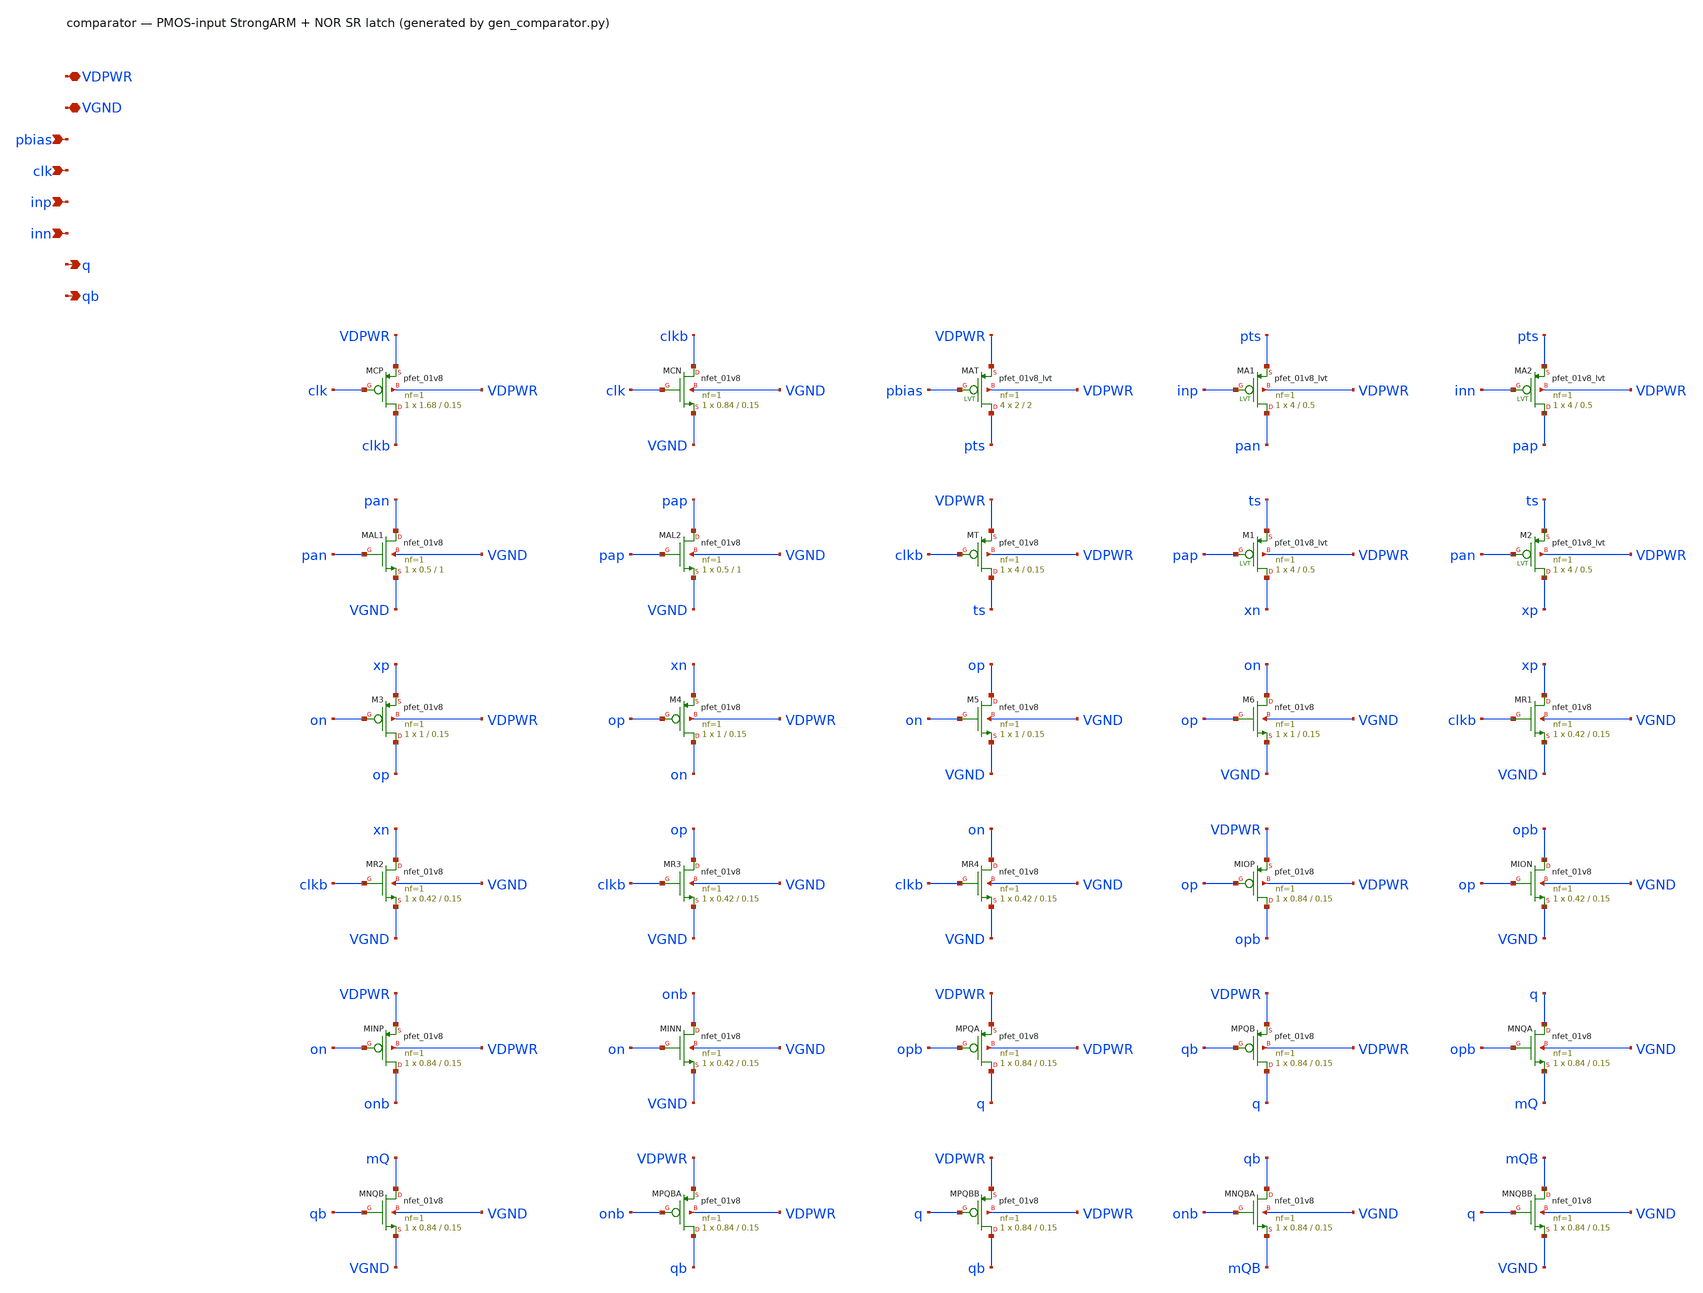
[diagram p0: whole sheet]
** sch_path: xschem/comparator.sch
**.subckt comparator VDPWR VGND pbias clk inp inn q qb
*.iopin VDPWR
*.iopin VGND
*.ipin pbias
*.ipin clk
*.ipin inp
*.ipin inn
*.opin q
*.opin qb
XMCP clkb clk VDPWR VDPWR sky130_fd_pr__pfet_01v8 L=0.15 W=1.68 nf=1 ad='int((nf+1)/2) * W/nf * 0.29'
+ as='int((nf+2)/2) * W/nf * 0.29' pd='2*int((nf+1)/2) * (W/nf + 0.29)' ps='2*int((nf+2)/2) * (W/nf + 0.29)'
+ nrd='0.29 / W' nrs='0.29 / W' sa=0 sb=0 sd=0 mult=1 m=1
XMCN clkb clk VGND VGND sky130_fd_pr__nfet_01v8 L=0.15 W=0.84 nf=1 ad='int((1 + 1)/2) * 0.84 / 1 * 0.29'
+ as='int((1 + 2)/2) * 0.84 / 1 * 0.29' pd='2*int((1 + 1)/2) * (0.84 / 1 + 0.29)' ps='2*int((1 + 2)/2) * (0.84 / 1 + 0.29)'
+ nrd='0.29 / 0.84 ' nrs='0.29 / 0.84 ' sa=0 sb=0 sd=0 mult=1 m=1
XMAT pts pbias VDPWR VDPWR sky130_fd_pr__pfet_01v8_lvt L=2 W=2 nf=1 ad='int((1 + 1)/2) * 2 / 1 * 0.29'
+ as='int((1 + 2)/2) * 2 / 1 * 0.29' pd='2*int((1 + 1)/2) * (2 / 1 + 0.29)' ps='2*int((1 + 2)/2) * (2 / 1 + 0.29)'
+ nrd='0.29 / 2 ' nrs='0.29 / 2 ' sa=0 sb=0 sd=0 mult=4 m=4
XMA1 pan inp pts VDPWR sky130_fd_pr__pfet_01v8_lvt L=0.5 W=4 nf=1 ad='int((1 + 1)/2) * 4 / 1 * 0.29'
+ as='int((1 + 2)/2) * 4 / 1 * 0.29' pd='2*int((1 + 1)/2) * (4 / 1 + 0.29)' ps='2*int((1 + 2)/2) * (4 / 1 + 0.29)'
+ nrd='0.29 / 4 ' nrs='0.29 / 4 ' sa=0 sb=0 sd=0 mult=1 m=1
XMA2 pap inn pts VDPWR sky130_fd_pr__pfet_01v8_lvt L=0.5 W=4 nf=1 ad='int((1 + 1)/2) * 4 / 1 * 0.29'
+ as='int((1 + 2)/2) * 4 / 1 * 0.29' pd='2*int((1 + 1)/2) * (4 / 1 + 0.29)' ps='2*int((1 + 2)/2) * (4 / 1 + 0.29)'
+ nrd='0.29 / 4 ' nrs='0.29 / 4 ' sa=0 sb=0 sd=0 mult=1 m=1
XMAL1 pan pan VGND VGND sky130_fd_pr__nfet_01v8 L=1 W=0.5 nf=1 ad='int((1 + 1)/2) * 0.5 / 1 * 0.29' as='int((1 + 2)/2) * 0.5 / 1 * 0.29'
+ pd='2*int((1 + 1)/2) * (0.5 / 1 + 0.29)' ps='2*int((1 + 2)/2) * (0.5 / 1 + 0.29)' nrd='0.29 / 0.5 ' nrs='0.29 / 0.5 '
+ sa=0 sb=0 sd=0 mult=1 m=1
XMAL2 pap pap VGND VGND sky130_fd_pr__nfet_01v8 L=1 W=0.5 nf=1 ad='int((1 + 1)/2) * 0.5 / 1 * 0.29' as='int((1 + 2)/2) * 0.5 / 1 * 0.29'
+ pd='2*int((1 + 1)/2) * (0.5 / 1 + 0.29)' ps='2*int((1 + 2)/2) * (0.5 / 1 + 0.29)' nrd='0.29 / 0.5 ' nrs='0.29 / 0.5 '
+ sa=0 sb=0 sd=0 mult=1 m=1
XMT ts clkb VDPWR VDPWR sky130_fd_pr__pfet_01v8 L=0.15 W=4 nf=1 ad='int((nf+1)/2) * W/nf * 0.29' as='int((nf+2)/2) * W/nf * 0.29'
+ pd='2*int((nf+1)/2) * (W/nf + 0.29)' ps='2*int((nf+2)/2) * (W/nf + 0.29)' nrd='0.29 / W' nrs='0.29 / W'
+ sa=0 sb=0 sd=0 mult=1 m=1
XM1 xn pap ts VDPWR sky130_fd_pr__pfet_01v8_lvt L=0.5 W=4 nf=1 ad='int((1 + 1)/2) * 4 / 1 * 0.29' as='int((1 + 2)/2) * 4 / 1 * 0.29'
+ pd='2*int((1 + 1)/2) * (4 / 1 + 0.29)' ps='2*int((1 + 2)/2) * (4 / 1 + 0.29)' nrd='0.29 / 4 ' nrs='0.29 / 4 '
+ sa=0 sb=0 sd=0 mult=1 m=1
XM2 xp pan ts VDPWR sky130_fd_pr__pfet_01v8_lvt L=0.5 W=4 nf=1 ad='int((1 + 1)/2) * 4 / 1 * 0.29' as='int((1 + 2)/2) * 4 / 1 * 0.29'
+ pd='2*int((1 + 1)/2) * (4 / 1 + 0.29)' ps='2*int((1 + 2)/2) * (4 / 1 + 0.29)' nrd='0.29 / 4 ' nrs='0.29 / 4 '
+ sa=0 sb=0 sd=0 mult=1 m=1
XM3 op on xp VDPWR sky130_fd_pr__pfet_01v8 L=0.15 W=1 nf=1 ad='int((nf+1)/2) * W/nf * 0.29' as='int((nf+2)/2) * W/nf * 0.29'
+ pd='2*int((nf+1)/2) * (W/nf + 0.29)' ps='2*int((nf+2)/2) * (W/nf + 0.29)' nrd='0.29 / W' nrs='0.29 / W'
+ sa=0 sb=0 sd=0 mult=1 m=1
XM4 on op xn VDPWR sky130_fd_pr__pfet_01v8 L=0.15 W=1 nf=1 ad='int((nf+1)/2) * W/nf * 0.29' as='int((nf+2)/2) * W/nf * 0.29'
+ pd='2*int((nf+1)/2) * (W/nf + 0.29)' ps='2*int((nf+2)/2) * (W/nf + 0.29)' nrd='0.29 / W' nrs='0.29 / W'
+ sa=0 sb=0 sd=0 mult=1 m=1
XM5 op on VGND VGND sky130_fd_pr__nfet_01v8 L=0.15 W=1 nf=1 ad='int((1 + 1)/2) * 1 / 1 * 0.29' as='int((1 + 2)/2) * 1 / 1 * 0.29'
+ pd='2*int((1 + 1)/2) * (1 / 1 + 0.29)' ps='2*int((1 + 2)/2) * (1 / 1 + 0.29)' nrd='0.29 / 1 ' nrs='0.29 / 1 '
+ sa=0 sb=0 sd=0 mult=1 m=1
XM6 on op VGND VGND sky130_fd_pr__nfet_01v8 L=0.15 W=1 nf=1 ad='int((1 + 1)/2) * 1 / 1 * 0.29' as='int((1 + 2)/2) * 1 / 1 * 0.29'
+ pd='2*int((1 + 1)/2) * (1 / 1 + 0.29)' ps='2*int((1 + 2)/2) * (1 / 1 + 0.29)' nrd='0.29 / 1 ' nrs='0.29 / 1 '
+ sa=0 sb=0 sd=0 mult=1 m=1
XMR1 xp clkb VGND VGND sky130_fd_pr__nfet_01v8 L=0.15 W=0.42 nf=1 ad='int((1 + 1)/2) * 0.42 / 1 * 0.29'
+ as='int((1 + 2)/2) * 0.42 / 1 * 0.29' pd='2*int((1 + 1)/2) * (0.42 / 1 + 0.29)' ps='2*int((1 + 2)/2) * (0.42 / 1 + 0.29)'
+ nrd='0.29 / 0.42 ' nrs='0.29 / 0.42 ' sa=0 sb=0 sd=0 mult=1 m=1
XMR2 xn clkb VGND VGND sky130_fd_pr__nfet_01v8 L=0.15 W=0.42 nf=1 ad='int((1 + 1)/2) * 0.42 / 1 * 0.29'
+ as='int((1 + 2)/2) * 0.42 / 1 * 0.29' pd='2*int((1 + 1)/2) * (0.42 / 1 + 0.29)' ps='2*int((1 + 2)/2) * (0.42 / 1 + 0.29)'
+ nrd='0.29 / 0.42 ' nrs='0.29 / 0.42 ' sa=0 sb=0 sd=0 mult=1 m=1
XMR3 op clkb VGND VGND sky130_fd_pr__nfet_01v8 L=0.15 W=0.42 nf=1 ad='int((1 + 1)/2) * 0.42 / 1 * 0.29'
+ as='int((1 + 2)/2) * 0.42 / 1 * 0.29' pd='2*int((1 + 1)/2) * (0.42 / 1 + 0.29)' ps='2*int((1 + 2)/2) * (0.42 / 1 + 0.29)'
+ nrd='0.29 / 0.42 ' nrs='0.29 / 0.42 ' sa=0 sb=0 sd=0 mult=1 m=1
XMR4 on clkb VGND VGND sky130_fd_pr__nfet_01v8 L=0.15 W=0.42 nf=1 ad='int((1 + 1)/2) * 0.42 / 1 * 0.29'
+ as='int((1 + 2)/2) * 0.42 / 1 * 0.29' pd='2*int((1 + 1)/2) * (0.42 / 1 + 0.29)' ps='2*int((1 + 2)/2) * (0.42 / 1 + 0.29)'
+ nrd='0.29 / 0.42 ' nrs='0.29 / 0.42 ' sa=0 sb=0 sd=0 mult=1 m=1
XMIOP opb op VDPWR VDPWR sky130_fd_pr__pfet_01v8 L=0.15 W=0.84 nf=1 ad='int((nf+1)/2) * W/nf * 0.29'
+ as='int((nf+2)/2) * W/nf * 0.29' pd='2*int((nf+1)/2) * (W/nf + 0.29)' ps='2*int((nf+2)/2) * (W/nf + 0.29)'
+ nrd='0.29 / W' nrs='0.29 / W' sa=0 sb=0 sd=0 mult=1 m=1
XMION opb op VGND VGND sky130_fd_pr__nfet_01v8 L=0.15 W=0.42 nf=1 ad='int((1 + 1)/2) * 0.42 / 1 * 0.29'
+ as='int((1 + 2)/2) * 0.42 / 1 * 0.29' pd='2*int((1 + 1)/2) * (0.42 / 1 + 0.29)' ps='2*int((1 + 2)/2) * (0.42 / 1 + 0.29)'
+ nrd='0.29 / 0.42 ' nrs='0.29 / 0.42 ' sa=0 sb=0 sd=0 mult=1 m=1
XMINP onb on VDPWR VDPWR sky130_fd_pr__pfet_01v8 L=0.15 W=0.84 nf=1 ad='int((nf+1)/2) * W/nf * 0.29'
+ as='int((nf+2)/2) * W/nf * 0.29' pd='2*int((nf+1)/2) * (W/nf + 0.29)' ps='2*int((nf+2)/2) * (W/nf + 0.29)'
+ nrd='0.29 / W' nrs='0.29 / W' sa=0 sb=0 sd=0 mult=1 m=1
XMINN onb on VGND VGND sky130_fd_pr__nfet_01v8 L=0.15 W=0.42 nf=1 ad='int((1 + 1)/2) * 0.42 / 1 * 0.29'
+ as='int((1 + 2)/2) * 0.42 / 1 * 0.29' pd='2*int((1 + 1)/2) * (0.42 / 1 + 0.29)' ps='2*int((1 + 2)/2) * (0.42 / 1 + 0.29)'
+ nrd='0.29 / 0.42 ' nrs='0.29 / 0.42 ' sa=0 sb=0 sd=0 mult=1 m=1
XMPQA q opb VDPWR VDPWR sky130_fd_pr__pfet_01v8 L=0.15 W=0.84 nf=1 ad='int((nf+1)/2) * W/nf * 0.29' as='int((nf+2)/2) * W/nf * 0.29'
+ pd='2*int((nf+1)/2) * (W/nf + 0.29)' ps='2*int((nf+2)/2) * (W/nf + 0.29)' nrd='0.29 / W' nrs='0.29 / W'
+ sa=0 sb=0 sd=0 mult=1 m=1
XMPQB q qb VDPWR VDPWR sky130_fd_pr__pfet_01v8 L=0.15 W=0.84 nf=1 ad='int((nf+1)/2) * W/nf * 0.29' as='int((nf+2)/2) * W/nf * 0.29'
+ pd='2*int((nf+1)/2) * (W/nf + 0.29)' ps='2*int((nf+2)/2) * (W/nf + 0.29)' nrd='0.29 / W' nrs='0.29 / W'
+ sa=0 sb=0 sd=0 mult=1 m=1
XMNQA q opb mQ VGND sky130_fd_pr__nfet_01v8 L=0.15 W=0.84 nf=1 ad='int((1 + 1)/2) * 0.84 / 1 * 0.29'
+ as='int((1 + 2)/2) * 0.84 / 1 * 0.29' pd='2*int((1 + 1)/2) * (0.84 / 1 + 0.29)' ps='2*int((1 + 2)/2) * (0.84 / 1 + 0.29)'
+ nrd='0.29 / 0.84 ' nrs='0.29 / 0.84 ' sa=0 sb=0 sd=0 mult=1 m=1
XMNQB mQ qb VGND VGND sky130_fd_pr__nfet_01v8 L=0.15 W=0.84 nf=1 ad='int((1 + 1)/2) * 0.84 / 1 * 0.29'
+ as='int((1 + 2)/2) * 0.84 / 1 * 0.29' pd='2*int((1 + 1)/2) * (0.84 / 1 + 0.29)' ps='2*int((1 + 2)/2) * (0.84 / 1 + 0.29)'
+ nrd='0.29 / 0.84 ' nrs='0.29 / 0.84 ' sa=0 sb=0 sd=0 mult=1 m=1
XMPQBA qb onb VDPWR VDPWR sky130_fd_pr__pfet_01v8 L=0.15 W=0.84 nf=1 ad='int((nf+1)/2) * W/nf * 0.29'
+ as='int((nf+2)/2) * W/nf * 0.29' pd='2*int((nf+1)/2) * (W/nf + 0.29)' ps='2*int((nf+2)/2) * (W/nf + 0.29)'
+ nrd='0.29 / W' nrs='0.29 / W' sa=0 sb=0 sd=0 mult=1 m=1
XMPQBB qb q VDPWR VDPWR sky130_fd_pr__pfet_01v8 L=0.15 W=0.84 nf=1 ad='int((nf+1)/2) * W/nf * 0.29' as='int((nf+2)/2) * W/nf * 0.29'
+ pd='2*int((nf+1)/2) * (W/nf + 0.29)' ps='2*int((nf+2)/2) * (W/nf + 0.29)' nrd='0.29 / W' nrs='0.29 / W'
+ sa=0 sb=0 sd=0 mult=1 m=1
XMNQBA qb onb mQB VGND sky130_fd_pr__nfet_01v8 L=0.15 W=0.84 nf=1 ad='int((1 + 1)/2) * 0.84 / 1 * 0.29'
+ as='int((1 + 2)/2) * 0.84 / 1 * 0.29' pd='2*int((1 + 1)/2) * (0.84 / 1 + 0.29)' ps='2*int((1 + 2)/2) * (0.84 / 1 + 0.29)'
+ nrd='0.29 / 0.84 ' nrs='0.29 / 0.84 ' sa=0 sb=0 sd=0 mult=1 m=1
XMNQBB mQB q VGND VGND sky130_fd_pr__nfet_01v8 L=0.15 W=0.84 nf=1 ad='int((1 + 1)/2) * 0.84 / 1 * 0.29'
+ as='int((1 + 2)/2) * 0.84 / 1 * 0.29' pd='2*int((1 + 1)/2) * (0.84 / 1 + 0.29)' ps='2*int((1 + 2)/2) * (0.84 / 1 + 0.29)'
+ nrd='0.29 / 0.84 ' nrs='0.29 / 0.84 ' sa=0 sb=0 sd=0 mult=1 m=1
**.ends
.end
